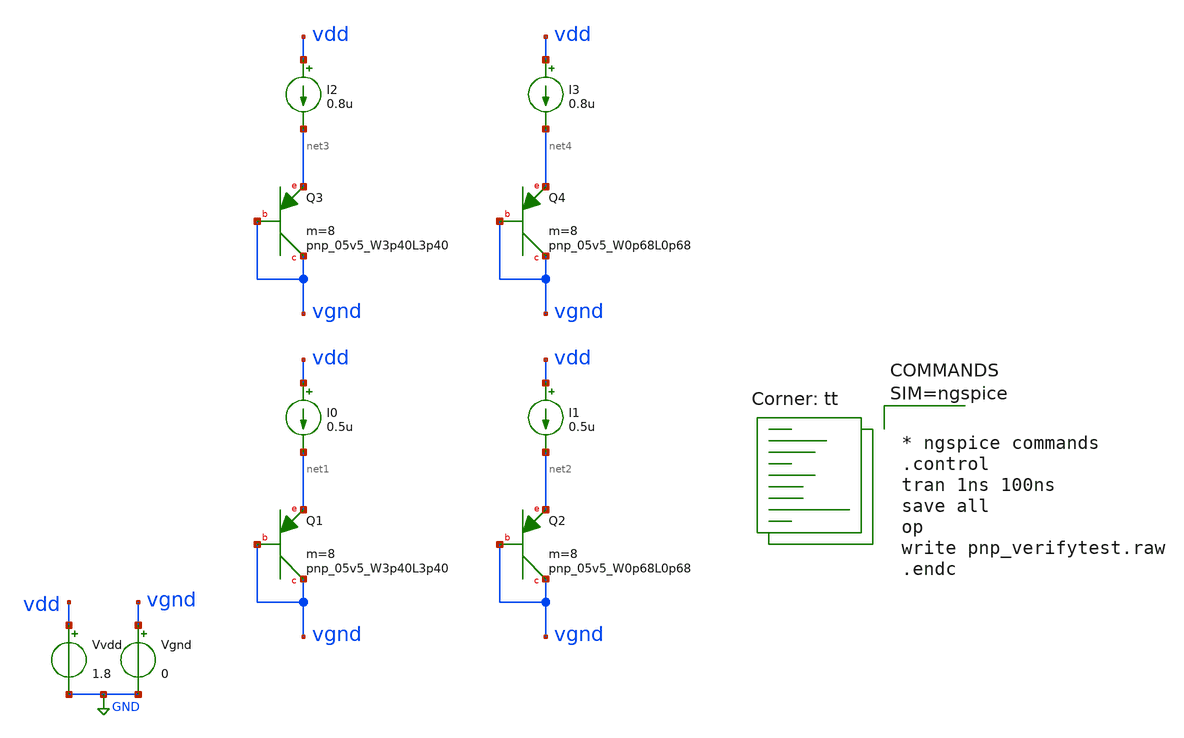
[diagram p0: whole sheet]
** sch_path: xschem/pnp_verifytest.sch
**.subckt pnp_verifytest
Vvdd vdd GND 1.8
Vgnd vgnd GND 0
XQ1 vgnd vgnd net1 sky130_fd_pr__pnp_05v5_W3p40L3p40 m=8
XQ2 vgnd vgnd net2 sky130_fd_pr__pnp_05v5_W0p68L0p68 m=8
I0 vdd net1 0.5u
I1 vdd net2 0.5u
XQ3 vgnd vgnd net3 sky130_fd_pr__pnp_05v5_W3p40L3p40 m=8
XQ4 vgnd vgnd net4 sky130_fd_pr__pnp_05v5_W0p68L0p68 m=8
I2 vdd net3 0.8u
I3 vdd net4 0.8u
**** begin user architecture code
.lib $::SKYWATER_MODELS/sky130.lib.spice tt



* ngspice commands
.control
tran 1ns 100ns
save all
op
write pnp_verifytest.raw
.endc



**** end user architecture code
**.ends
.GLOBAL GND
.end
